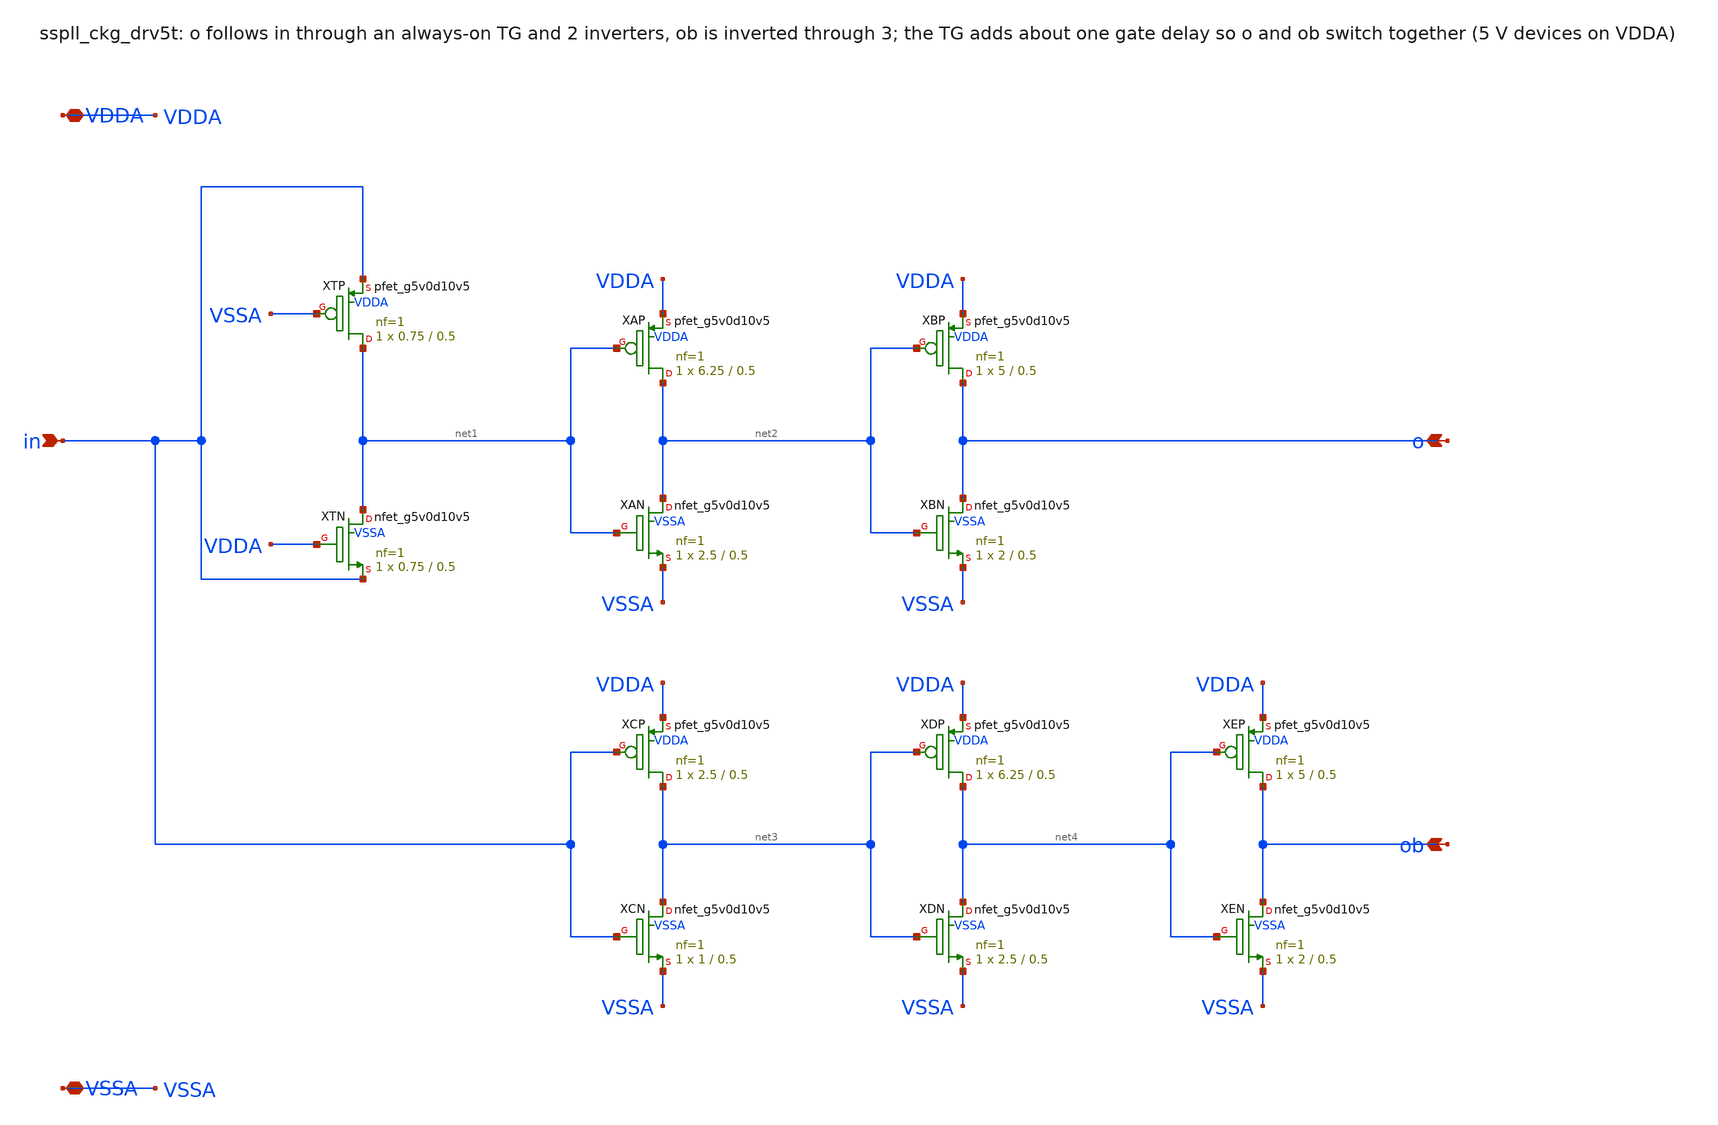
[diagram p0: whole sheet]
** sch_path: xschem/clkgen_hv/sspll_ckg_drv5t.sch
**.subckt sspll_ckg_drv5t in o ob VDDA VSSA
*.ipin in
*.opin o
*.opin ob
*.iopin VDDA
*.iopin VSSA
XXTN net1 VDDA in VSSA sky130_fd_pr__nfet_g5v0d10v5 L=0.5 W=0.75 nf=1 ad='int((nf+1)/2) * W/nf * 0.29'
+ as='int((nf+2)/2) * W/nf * 0.29' pd='2*int((nf+1)/2) * (W/nf + 0.29)' ps='2*int((nf+2)/2) * (W/nf + 0.29)'
+ nrd='0.29 / W' nrs='0.29 / W' sa=0 sb=0 sd=0 mult=1 m=1
XXTP net1 VSSA in VDDA sky130_fd_pr__pfet_g5v0d10v5 L=0.5 W=0.75 nf=1 ad='int((nf+1)/2) * W/nf * 0.29'
+ as='int((nf+2)/2) * W/nf * 0.29' pd='2*int((nf+1)/2) * (W/nf + 0.29)' ps='2*int((nf+2)/2) * (W/nf + 0.29)'
+ nrd='0.29 / W' nrs='0.29 / W' sa=0 sb=0 sd=0 mult=1 m=1
XXAP net2 net1 VDDA VDDA sky130_fd_pr__pfet_g5v0d10v5 L=0.5 W=6.25 nf=1 ad='int((nf+1)/2) * W/nf * 0.29'
+ as='int((nf+2)/2) * W/nf * 0.29' pd='2*int((nf+1)/2) * (W/nf + 0.29)' ps='2*int((nf+2)/2) * (W/nf + 0.29)'
+ nrd='0.29 / W' nrs='0.29 / W' sa=0 sb=0 sd=0 mult=1 m=1
XXAN net2 net1 VSSA VSSA sky130_fd_pr__nfet_g5v0d10v5 L=0.5 W=2.5 nf=1 ad='int((nf+1)/2) * W/nf * 0.29'
+ as='int((nf+2)/2) * W/nf * 0.29' pd='2*int((nf+1)/2) * (W/nf + 0.29)' ps='2*int((nf+2)/2) * (W/nf + 0.29)'
+ nrd='0.29 / W' nrs='0.29 / W' sa=0 sb=0 sd=0 mult=1 m=1
XXBP o net2 VDDA VDDA sky130_fd_pr__pfet_g5v0d10v5 L=0.5 W=5 nf=1 ad='int((nf+1)/2) * W/nf * 0.29' as='int((nf+2)/2) * W/nf * 0.29'
+ pd='2*int((nf+1)/2) * (W/nf + 0.29)' ps='2*int((nf+2)/2) * (W/nf + 0.29)' nrd='0.29 / W' nrs='0.29 / W'
+ sa=0 sb=0 sd=0 mult=1 m=1
XXBN o net2 VSSA VSSA sky130_fd_pr__nfet_g5v0d10v5 L=0.5 W=2 nf=1 ad='int((nf+1)/2) * W/nf * 0.29' as='int((nf+2)/2) * W/nf * 0.29'
+ pd='2*int((nf+1)/2) * (W/nf + 0.29)' ps='2*int((nf+2)/2) * (W/nf + 0.29)' nrd='0.29 / W' nrs='0.29 / W'
+ sa=0 sb=0 sd=0 mult=1 m=1
XXCP net3 in VDDA VDDA sky130_fd_pr__pfet_g5v0d10v5 L=0.5 W=2.5 nf=1 ad='int((nf+1)/2) * W/nf * 0.29'
+ as='int((nf+2)/2) * W/nf * 0.29' pd='2*int((nf+1)/2) * (W/nf + 0.29)' ps='2*int((nf+2)/2) * (W/nf + 0.29)'
+ nrd='0.29 / W' nrs='0.29 / W' sa=0 sb=0 sd=0 mult=1 m=1
XXCN net3 in VSSA VSSA sky130_fd_pr__nfet_g5v0d10v5 L=0.5 W=1 nf=1 ad='int((nf+1)/2) * W/nf * 0.29' as='int((nf+2)/2) * W/nf * 0.29'
+ pd='2*int((nf+1)/2) * (W/nf + 0.29)' ps='2*int((nf+2)/2) * (W/nf + 0.29)' nrd='0.29 / W' nrs='0.29 / W'
+ sa=0 sb=0 sd=0 mult=1 m=1
XXDP net4 net3 VDDA VDDA sky130_fd_pr__pfet_g5v0d10v5 L=0.5 W=6.25 nf=1 ad='int((nf+1)/2) * W/nf * 0.29'
+ as='int((nf+2)/2) * W/nf * 0.29' pd='2*int((nf+1)/2) * (W/nf + 0.29)' ps='2*int((nf+2)/2) * (W/nf + 0.29)'
+ nrd='0.29 / W' nrs='0.29 / W' sa=0 sb=0 sd=0 mult=1 m=1
XXDN net4 net3 VSSA VSSA sky130_fd_pr__nfet_g5v0d10v5 L=0.5 W=2.5 nf=1 ad='int((nf+1)/2) * W/nf * 0.29'
+ as='int((nf+2)/2) * W/nf * 0.29' pd='2*int((nf+1)/2) * (W/nf + 0.29)' ps='2*int((nf+2)/2) * (W/nf + 0.29)'
+ nrd='0.29 / W' nrs='0.29 / W' sa=0 sb=0 sd=0 mult=1 m=1
XXEP ob net4 VDDA VDDA sky130_fd_pr__pfet_g5v0d10v5 L=0.5 W=5 nf=1 ad='int((nf+1)/2) * W/nf * 0.29' as='int((nf+2)/2) * W/nf * 0.29'
+ pd='2*int((nf+1)/2) * (W/nf + 0.29)' ps='2*int((nf+2)/2) * (W/nf + 0.29)' nrd='0.29 / W' nrs='0.29 / W'
+ sa=0 sb=0 sd=0 mult=1 m=1
XXEN ob net4 VSSA VSSA sky130_fd_pr__nfet_g5v0d10v5 L=0.5 W=2 nf=1 ad='int((nf+1)/2) * W/nf * 0.29' as='int((nf+2)/2) * W/nf * 0.29'
+ pd='2*int((nf+1)/2) * (W/nf + 0.29)' ps='2*int((nf+2)/2) * (W/nf + 0.29)' nrd='0.29 / W' nrs='0.29 / W'
+ sa=0 sb=0 sd=0 mult=1 m=1
**.ends
.end
